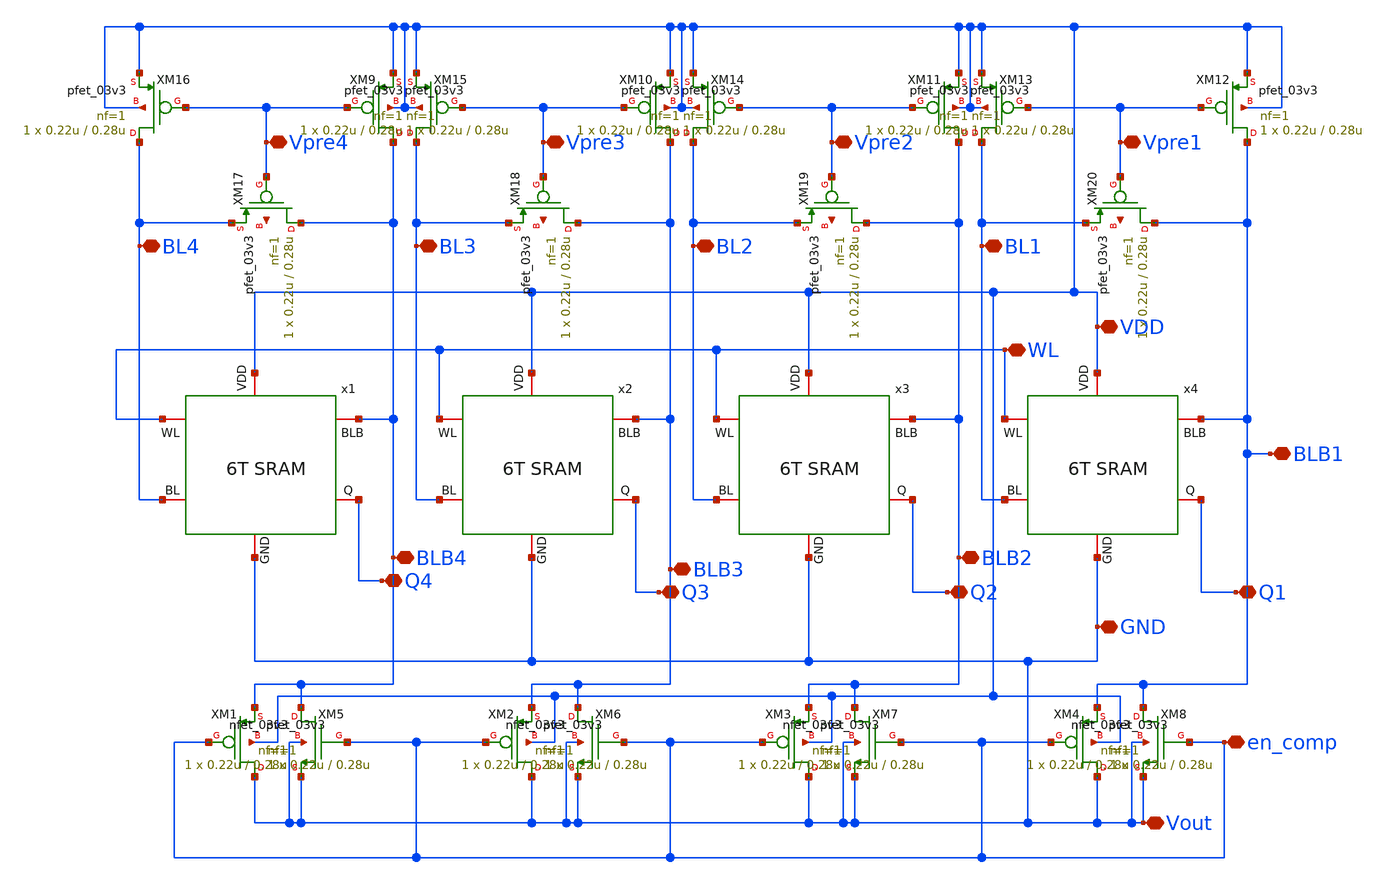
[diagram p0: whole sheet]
** sch_path: src/schematic/MEMORY/memori.sch
**.subckt memori GND VDD WL Q1 Q2 Q3 Q4 Vpre4 Vpre3 Vpre2 Vpre1 en_comp Vout BLB1 BLB2 BLB3 BLB4 BL1
*+ BL2 BL3 BL4
*.iopin GND
*.iopin VDD
*.iopin WL
*.iopin Q1
*.iopin Q2
*.iopin Q3
*.iopin Q4
*.iopin Vpre4
*.iopin Vpre3
*.iopin Vpre2
*.iopin Vpre1
*.iopin en_comp
*.iopin Vout
*.iopin BLB1
*.iopin BLB2
*.iopin BLB3
*.iopin BLB4
*.iopin BL1
*.iopin BL2
*.iopin BL3
*.iopin BL4
x1 VDD WL BLB4 BL4 Q4 GND 6T4bit
x2 VDD WL BLB3 BL3 Q3 GND 6T4bit
x3 VDD WL BLB2 BL2 Q2 GND 6T4bit
x4 VDD WL BLB1 BL1 Q1 GND 6T4bit
XM1 GND en_comp BLB4 VDD pfet_03v3 L=0.28u W=0.22u nf=1 ad='int((nf+1)/2) * W/nf * 0.18u' as='int((nf+2)/2) * W/nf * 0.18u'
+ pd='2*int((nf+1)/2) * (W/nf + 0.18u)' ps='2*int((nf+2)/2) * (W/nf + 0.18u)' nrd='0.18u / W' nrs='0.18u / W'
+ sa=0 sb=0 sd=0 m=1
XM2 GND en_comp BLB3 VDD pfet_03v3 L=0.28u W=0.22u nf=1 ad='int((nf+1)/2) * W/nf * 0.18u' as='int((nf+2)/2) * W/nf * 0.18u'
+ pd='2*int((nf+1)/2) * (W/nf + 0.18u)' ps='2*int((nf+2)/2) * (W/nf + 0.18u)' nrd='0.18u / W' nrs='0.18u / W'
+ sa=0 sb=0 sd=0 m=1
XM3 GND en_comp BLB2 VDD pfet_03v3 L=0.28u W=0.22u nf=1 ad='int((nf+1)/2) * W/nf * 0.18u' as='int((nf+2)/2) * W/nf * 0.18u'
+ pd='2*int((nf+1)/2) * (W/nf + 0.18u)' ps='2*int((nf+2)/2) * (W/nf + 0.18u)' nrd='0.18u / W' nrs='0.18u / W'
+ sa=0 sb=0 sd=0 m=1
XM4 GND en_comp BLB1 VDD pfet_03v3 L=0.28u W=0.22u nf=1 ad='int((nf+1)/2) * W/nf * 0.18u' as='int((nf+2)/2) * W/nf * 0.18u'
+ pd='2*int((nf+1)/2) * (W/nf + 0.18u)' ps='2*int((nf+2)/2) * (W/nf + 0.18u)' nrd='0.18u / W' nrs='0.18u / W'
+ sa=0 sb=0 sd=0 m=1
XM5 BLB4 en_comp GND GND nfet_03v3 L=0.28u W=0.22u nf=1 ad='int((nf+1)/2) * W/nf * 0.18u' as='int((nf+2)/2) * W/nf * 0.18u'
+ pd='2*int((nf+1)/2) * (W/nf + 0.18u)' ps='2*int((nf+2)/2) * (W/nf + 0.18u)' nrd='0.18u / W' nrs='0.18u / W'
+ sa=0 sb=0 sd=0 m=1
XM6 BLB3 en_comp GND GND nfet_03v3 L=0.28u W=0.22u nf=1 ad='int((nf+1)/2) * W/nf * 0.18u' as='int((nf+2)/2) * W/nf * 0.18u'
+ pd='2*int((nf+1)/2) * (W/nf + 0.18u)' ps='2*int((nf+2)/2) * (W/nf + 0.18u)' nrd='0.18u / W' nrs='0.18u / W'
+ sa=0 sb=0 sd=0 m=1
XM7 BLB2 en_comp GND GND nfet_03v3 L=0.28u W=0.22u nf=1 ad='int((nf+1)/2) * W/nf * 0.18u' as='int((nf+2)/2) * W/nf * 0.18u'
+ pd='2*int((nf+1)/2) * (W/nf + 0.18u)' ps='2*int((nf+2)/2) * (W/nf + 0.18u)' nrd='0.18u / W' nrs='0.18u / W'
+ sa=0 sb=0 sd=0 m=1
XM8 BLB1 en_comp GND GND nfet_03v3 L=0.28u W=0.22u nf=1 ad='int((nf+1)/2) * W/nf * 0.18u' as='int((nf+2)/2) * W/nf * 0.18u'
+ pd='2*int((nf+1)/2) * (W/nf + 0.18u)' ps='2*int((nf+2)/2) * (W/nf + 0.18u)' nrd='0.18u / W' nrs='0.18u / W'
+ sa=0 sb=0 sd=0 m=1
XM9 BLB4 Vpre4 VDD VDD pfet_03v3 L=0.28u W=0.22u nf=1 ad='int((nf+1)/2) * W/nf * 0.18u' as='int((nf+2)/2) * W/nf * 0.18u'
+ pd='2*int((nf+1)/2) * (W/nf + 0.18u)' ps='2*int((nf+2)/2) * (W/nf + 0.18u)' nrd='0.18u / W' nrs='0.18u / W'
+ sa=0 sb=0 sd=0 m=1
XM10 BLB3 Vpre3 VDD VDD pfet_03v3 L=0.28u W=0.22u nf=1 ad='int((nf+1)/2) * W/nf * 0.18u' as='int((nf+2)/2) * W/nf * 0.18u'
+ pd='2*int((nf+1)/2) * (W/nf + 0.18u)' ps='2*int((nf+2)/2) * (W/nf + 0.18u)' nrd='0.18u / W' nrs='0.18u / W'
+ sa=0 sb=0 sd=0 m=1
XM11 BLB2 Vpre2 VDD VDD pfet_03v3 L=0.28u W=0.22u nf=1 ad='int((nf+1)/2) * W/nf * 0.18u' as='int((nf+2)/2) * W/nf * 0.18u'
+ pd='2*int((nf+1)/2) * (W/nf + 0.18u)' ps='2*int((nf+2)/2) * (W/nf + 0.18u)' nrd='0.18u / W' nrs='0.18u / W'
+ sa=0 sb=0 sd=0 m=1
XM12 BLB1 Vpre1 VDD VDD pfet_03v3 L=0.28u W=0.22u nf=1 ad='int((nf+1)/2) * W/nf * 0.18u' as='int((nf+2)/2) * W/nf * 0.18u'
+ pd='2*int((nf+1)/2) * (W/nf + 0.18u)' ps='2*int((nf+2)/2) * (W/nf + 0.18u)' nrd='0.18u / W' nrs='0.18u / W'
+ sa=0 sb=0 sd=0 m=1
XM13 BL1 Vpre1 VDD VDD pfet_03v3 L=0.28u W=0.22u nf=1 ad='int((nf+1)/2) * W/nf * 0.18u' as='int((nf+2)/2) * W/nf * 0.18u'
+ pd='2*int((nf+1)/2) * (W/nf + 0.18u)' ps='2*int((nf+2)/2) * (W/nf + 0.18u)' nrd='0.18u / W' nrs='0.18u / W'
+ sa=0 sb=0 sd=0 m=1
XM14 BL2 Vpre2 VDD VDD pfet_03v3 L=0.28u W=0.22u nf=1 ad='int((nf+1)/2) * W/nf * 0.18u' as='int((nf+2)/2) * W/nf * 0.18u'
+ pd='2*int((nf+1)/2) * (W/nf + 0.18u)' ps='2*int((nf+2)/2) * (W/nf + 0.18u)' nrd='0.18u / W' nrs='0.18u / W'
+ sa=0 sb=0 sd=0 m=1
XM15 BL3 Vpre3 VDD VDD pfet_03v3 L=0.28u W=0.22u nf=1 ad='int((nf+1)/2) * W/nf * 0.18u' as='int((nf+2)/2) * W/nf * 0.18u'
+ pd='2*int((nf+1)/2) * (W/nf + 0.18u)' ps='2*int((nf+2)/2) * (W/nf + 0.18u)' nrd='0.18u / W' nrs='0.18u / W'
+ sa=0 sb=0 sd=0 m=1
XM16 BL4 Vpre4 VDD VDD pfet_03v3 L=0.28u W=0.22u nf=1 ad='int((nf+1)/2) * W/nf * 0.18u' as='int((nf+2)/2) * W/nf * 0.18u'
+ pd='2*int((nf+1)/2) * (W/nf + 0.18u)' ps='2*int((nf+2)/2) * (W/nf + 0.18u)' nrd='0.18u / W' nrs='0.18u / W'
+ sa=0 sb=0 sd=0 m=1
XM17 BLB4 Vpre4 BL4 net1 pfet_03v3 L=0.28u W=0.22u nf=1 ad='int((nf+1)/2) * W/nf * 0.18u' as='int((nf+2)/2) * W/nf * 0.18u'
+ pd='2*int((nf+1)/2) * (W/nf + 0.18u)' ps='2*int((nf+2)/2) * (W/nf + 0.18u)' nrd='0.18u / W' nrs='0.18u / W'
+ sa=0 sb=0 sd=0 m=1
XM18 BLB3 Vpre3 BL3 net2 pfet_03v3 L=0.28u W=0.22u nf=1 ad='int((nf+1)/2) * W/nf * 0.18u' as='int((nf+2)/2) * W/nf * 0.18u'
+ pd='2*int((nf+1)/2) * (W/nf + 0.18u)' ps='2*int((nf+2)/2) * (W/nf + 0.18u)' nrd='0.18u / W' nrs='0.18u / W'
+ sa=0 sb=0 sd=0 m=1
XM19 BLB2 Vpre2 BL2 net3 pfet_03v3 L=0.28u W=0.22u nf=1 ad='int((nf+1)/2) * W/nf * 0.18u' as='int((nf+2)/2) * W/nf * 0.18u'
+ pd='2*int((nf+1)/2) * (W/nf + 0.18u)' ps='2*int((nf+2)/2) * (W/nf + 0.18u)' nrd='0.18u / W' nrs='0.18u / W'
+ sa=0 sb=0 sd=0 m=1
XM20 BLB1 Vpre1 BL1 net4 pfet_03v3 L=0.28u W=0.22u nf=1 ad='int((nf+1)/2) * W/nf * 0.18u' as='int((nf+2)/2) * W/nf * 0.18u'
+ pd='2*int((nf+1)/2) * (W/nf + 0.18u)' ps='2*int((nf+2)/2) * (W/nf + 0.18u)' nrd='0.18u / W' nrs='0.18u / W'
+ sa=0 sb=0 sd=0 m=1
**.ends

* expanding   symbol:  6T4bit.sym # of pins=6
** sym_path: src/schematic/MEMORY/6T4bit.sym
** sch_path: src/schematic/MEMORY/6T4bit.sch
.subckt 6T4bit VDD WL BLB BL Q GND
*.iopin BLB
*.iopin GND
*.iopin Q
*.iopin VDD
*.iopin BL
*.iopin WL
XSR1_M6 Q WL BL GND nfet_03v3 L=0.28u W=0.22u nf=1 ad='int((nf+1)/2) * W/nf * 0.18u' as='int((nf+2)/2) * W/nf * 0.18u'
+ pd='2*int((nf+1)/2) * (W/nf + 0.18u)' ps='2*int((nf+2)/2) * (W/nf + 0.18u)' nrd='0.18u / W' nrs='0.18u / W'
+ sa=0 sb=0 sd=0 m=1
XSR1_M3 Q net1 Q Q pfet_03v3 L=0.28u W=0.22u nf=1 ad='int((nf+1)/2) * W/nf * 0.18u' as='int((nf+2)/2) * W/nf * 0.18u'
+ pd='2*int((nf+1)/2) * (W/nf + 0.18u)' ps='2*int((nf+2)/2) * (W/nf + 0.18u)' nrd='0.18u / W' nrs='0.18u / W'
+ sa=0 sb=0 sd=0 m=1
XSR1_M4 net1 Q Q Q pfet_03v3 L=0.28u W=0.22u nf=1 ad='int((nf+1)/2) * W/nf * 0.18u' as='int((nf+2)/2) * W/nf * 0.18u'
+ pd='2*int((nf+1)/2) * (W/nf + 0.18u)' ps='2*int((nf+2)/2) * (W/nf + 0.18u)' nrd='0.18u / W' nrs='0.18u / W'
+ sa=0 sb=0 sd=0 m=1
XSR1_M5 BLB WL net1 GND nfet_03v3 L=0.28u W=0.22u nf=1 ad='int((nf+1)/2) * W/nf * 0.18u' as='int((nf+2)/2) * W/nf * 0.18u'
+ pd='2*int((nf+1)/2) * (W/nf + 0.18u)' ps='2*int((nf+2)/2) * (W/nf + 0.18u)' nrd='0.18u / W' nrs='0.18u / W'
+ sa=0 sb=0 sd=0 m=1
XSR1_M1 Q net1 GND GND nfet_03v3 L=0.28u W=0.22u nf=1 ad='int((nf+1)/2) * W/nf * 0.18u' as='int((nf+2)/2) * W/nf * 0.18u'
+ pd='2*int((nf+1)/2) * (W/nf + 0.18u)' ps='2*int((nf+2)/2) * (W/nf + 0.18u)' nrd='0.18u / W' nrs='0.18u / W'
+ sa=0 sb=0 sd=0 m=1
XSR1_M2 net1 Q GND GND nfet_03v3 L=0.28u W=0.22u nf=1 ad='int((nf+1)/2) * W/nf * 0.18u' as='int((nf+2)/2) * W/nf * 0.18u'
+ pd='2*int((nf+1)/2) * (W/nf + 0.18u)' ps='2*int((nf+2)/2) * (W/nf + 0.18u)' nrd='0.18u / W' nrs='0.18u / W'
+ sa=0 sb=0 sd=0 m=1
.ends

.end
